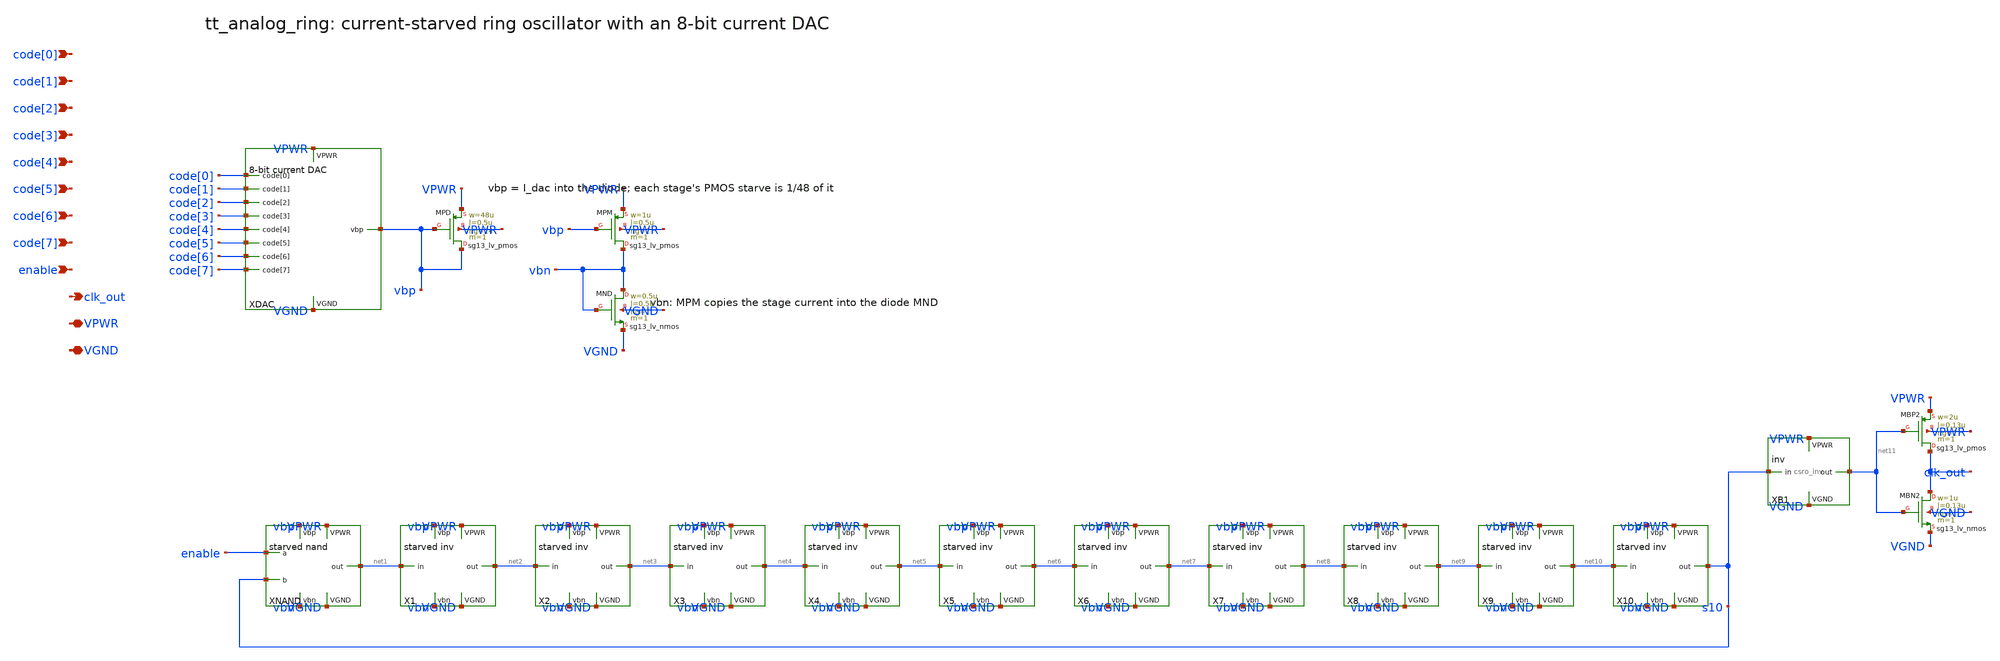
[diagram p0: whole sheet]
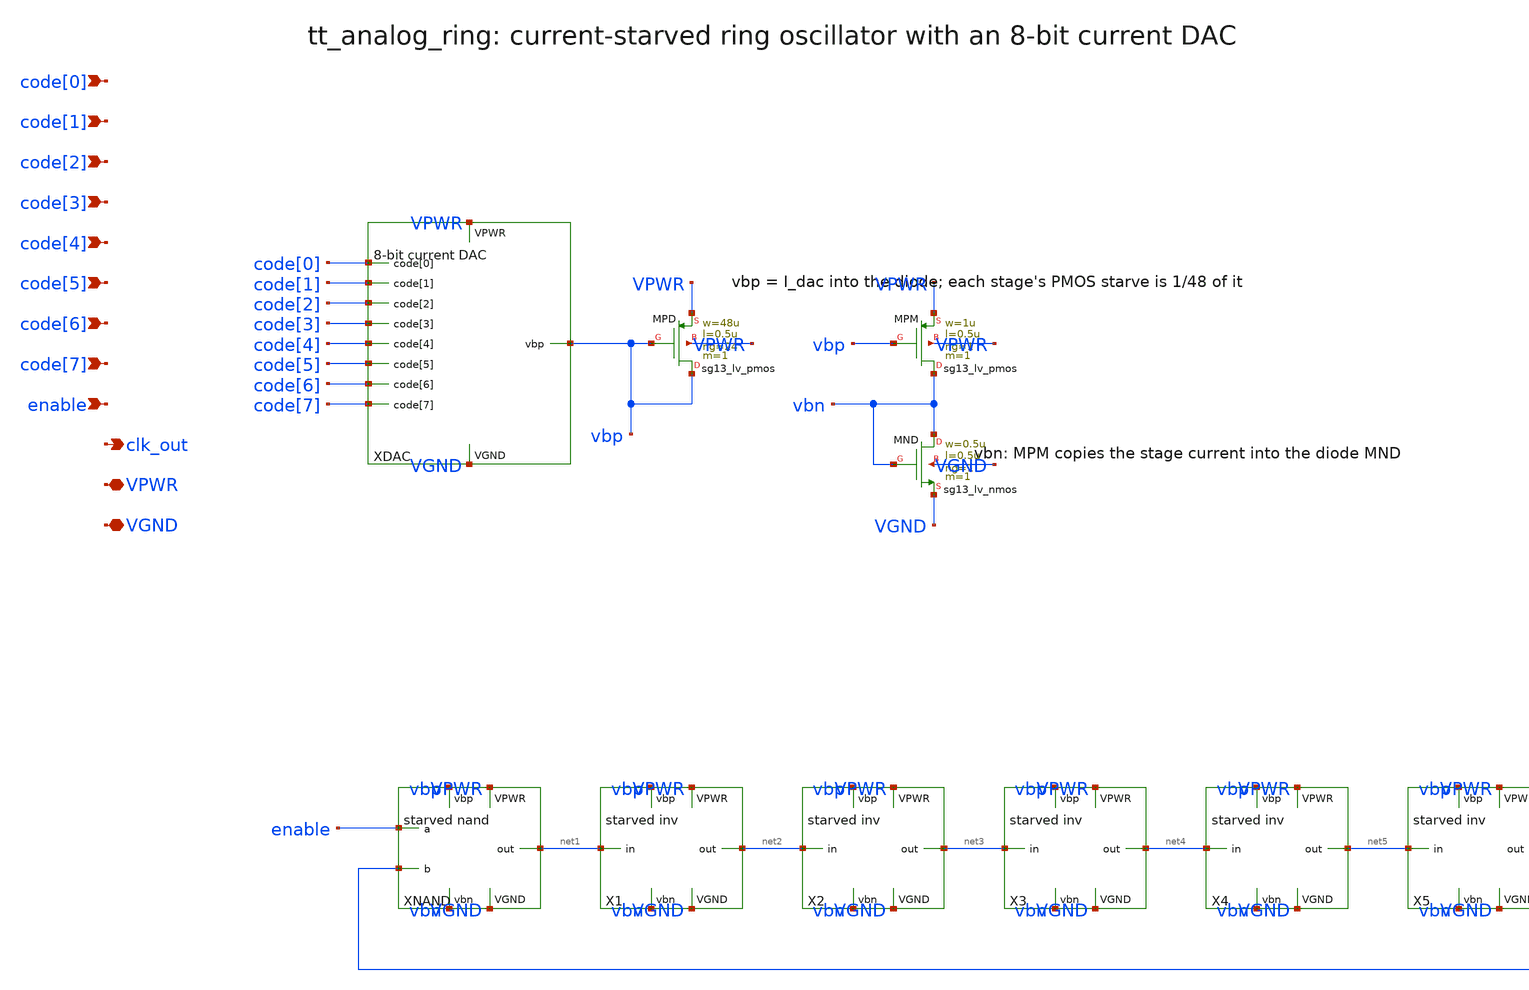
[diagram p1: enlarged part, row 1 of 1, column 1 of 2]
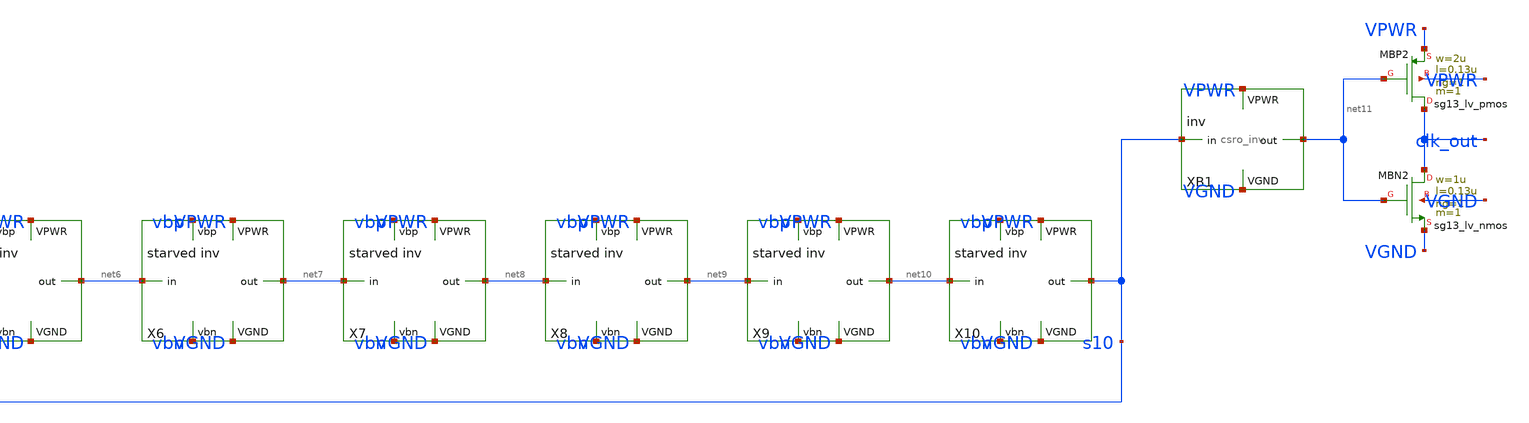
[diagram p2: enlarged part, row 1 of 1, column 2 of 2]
** sch_path: analog/xschem/tt_analog_ring.sch
**.subckt tt_analog_ring code[0] code[1] code[2] code[3] code[4] code[5] code[6] code[7] enable
*+ clk_out VPWR VGND
*.ipin code[0]
*.ipin code[1]
*.ipin code[2]
*.ipin code[3]
*.ipin code[4]
*.ipin code[5]
*.ipin code[6]
*.ipin code[7]
*.ipin enable
*.opin clk_out
*.iopin VPWR
*.iopin VGND
XDAC code[0] code[1] code[2] code[3] code[4] code[5] code[6] code[7] vbp VPWR VGND csro_dac
XMPD vbp vbp VPWR VPWR sg13_lv_pmos w=48u l=0.5u ng=24 m=1 mm_ok=1
XMPM vbn vbp VPWR VPWR sg13_lv_pmos w=1u l=0.5u ng=1 m=1 mm_ok=1
XMND vbn vbn VGND VGND sg13_lv_nmos w=0.5u l=0.5u ng=1 m=1 mm_ok=1
XNAND enable s10 net1 vbp VPWR vbn VGND csro_nand
X1 net1 net2 vbp VPWR vbn VGND csro_stage
X2 net2 net3 vbp VPWR vbn VGND csro_stage
X3 net3 net4 vbp VPWR vbn VGND csro_stage
X4 net4 net5 vbp VPWR vbn VGND csro_stage
X5 net5 net6 vbp VPWR vbn VGND csro_stage
X6 net6 net7 vbp VPWR vbn VGND csro_stage
X7 net7 net8 vbp VPWR vbn VGND csro_stage
X8 net8 net9 vbp VPWR vbn VGND csro_stage
X9 net9 net10 vbp VPWR vbn VGND csro_stage
X10 net10 s10 vbp VPWR vbn VGND csro_stage
XB1 s10 net11 VPWR VGND csro_inv
XMBP2 clk_out net11 VPWR VPWR sg13_lv_pmos w=2u l=0.13u ng=1 m=1 mm_ok=1
XMBN2 clk_out net11 VGND VGND sg13_lv_nmos w=1u l=0.13u ng=1 m=1 mm_ok=1
**.ends

* expanding   symbol:  csro_dac.sym # of pins=11
** sym_path: analog/xschem/csro_dac.sym
** sch_path: analog/xschem/csro_dac.sch
.subckt csro_dac code[0] code[1] code[2] code[3] code[4] code[5] code[6] code[7] vbp VPWR VGND
*.ipin code[0]
*.ipin code[1]
*.ipin code[2]
*.ipin code[3]
*.ipin code[4]
*.ipin code[5]
*.ipin code[6]
*.ipin code[7]
*.opin vbp
*.iopin VPWR
*.iopin VGND
XD0 vbp code[0] VGND VGND sg13_lv_nmos w=0.15u l=8u ng=1 m=1 mm_ok=1
XD1 vbp code[1] VGND VGND sg13_lv_nmos w=0.3u l=8u ng=2 m=1 mm_ok=1
XD2 vbp code[2] VGND VGND sg13_lv_nmos w=0.6u l=8u ng=4 m=1 mm_ok=1
XD3 vbp code[3] VGND VGND sg13_lv_nmos w=1.2u l=8u ng=8 m=1 mm_ok=1
XD4 vbp code[4] VGND VGND sg13_lv_nmos w=2.4u l=8u ng=16 m=1 mm_ok=1
XD5 vbp code[5] VGND VGND sg13_lv_nmos w=4.8u l=8u ng=32 m=1 mm_ok=1
XD6 vbp code[6] VGND VGND sg13_lv_nmos w=9.6u l=8u ng=64 m=1 mm_ok=1
XD7 vbp code[7] VGND VGND sg13_lv_nmos w=19.2u l=8u ng=128 m=1 mm_ok=1
XDON vbp VPWR VGND VGND sg13_lv_nmos w=0.3u l=8u ng=2 m=1 mm_ok=1
.ends


* expanding   symbol:  csro_nand.sym # of pins=7
** sym_path: analog/xschem/csro_nand.sym
** sch_path: analog/xschem/csro_nand.sch
.subckt csro_nand a b out vbp VPWR vbn VGND
*.ipin a
*.ipin b
*.opin out
*.ipin vbp
*.iopin VPWR
*.ipin vbn
*.iopin VGND
XMPS0 net1 vbp VPWR VPWR sg13_lv_pmos w=1u l=0.5u ng=1 m=1 mm_ok=1
XMPA0 out a net1 VPWR sg13_lv_pmos w=0.5u l=0.13u ng=1 m=1 mm_ok=1
XMPB0 out b net1 VPWR sg13_lv_pmos w=0.5u l=0.13u ng=1 m=1 mm_ok=1
XMNB0 out b net2 VGND sg13_lv_nmos w=0.6u l=0.13u ng=1 m=1 mm_ok=1
XMNA0 net2 a net3 VGND sg13_lv_nmos w=0.6u l=0.13u ng=1 m=1 mm_ok=1
XMNS0 net3 vbn VGND VGND sg13_lv_nmos w=0.5u l=0.5u ng=1 m=1 mm_ok=1
.ends


* expanding   symbol:  csro_stage.sym # of pins=6
** sym_path: analog/xschem/csro_stage.sym
** sch_path: analog/xschem/csro_stage.sch
.subckt csro_stage in out vbp VPWR vbn VGND
*.ipin in
*.opin out
*.ipin vbp
*.iopin VPWR
*.ipin vbn
*.iopin VGND
XMPS net1 vbp VPWR VPWR sg13_lv_pmos w=1u l=0.5u ng=1 m=1 mm_ok=1
XMP out in net1 VPWR sg13_lv_pmos w=0.5u l=0.13u ng=1 m=1 mm_ok=1
XMN out in net2 VGND sg13_lv_nmos w=0.3u l=0.13u ng=1 m=1 mm_ok=1
XMNS net2 vbn VGND VGND sg13_lv_nmos w=0.5u l=0.5u ng=1 m=1 mm_ok=1
.ends


* expanding   symbol:  csro_inv.sym # of pins=4
** sym_path: analog/xschem/csro_inv.sym
** sch_path: analog/xschem/csro_inv.sch
.subckt csro_inv in out VPWR VGND
*.ipin in
*.opin out
*.iopin VPWR
*.iopin VGND
XMBP out in VPWR VPWR sg13_lv_pmos w=0.5u l=0.13u ng=1 m=1 mm_ok=1
XMBN out in VGND VGND sg13_lv_nmos w=0.3u l=0.13u ng=1 m=1 mm_ok=1
.ends

.end
